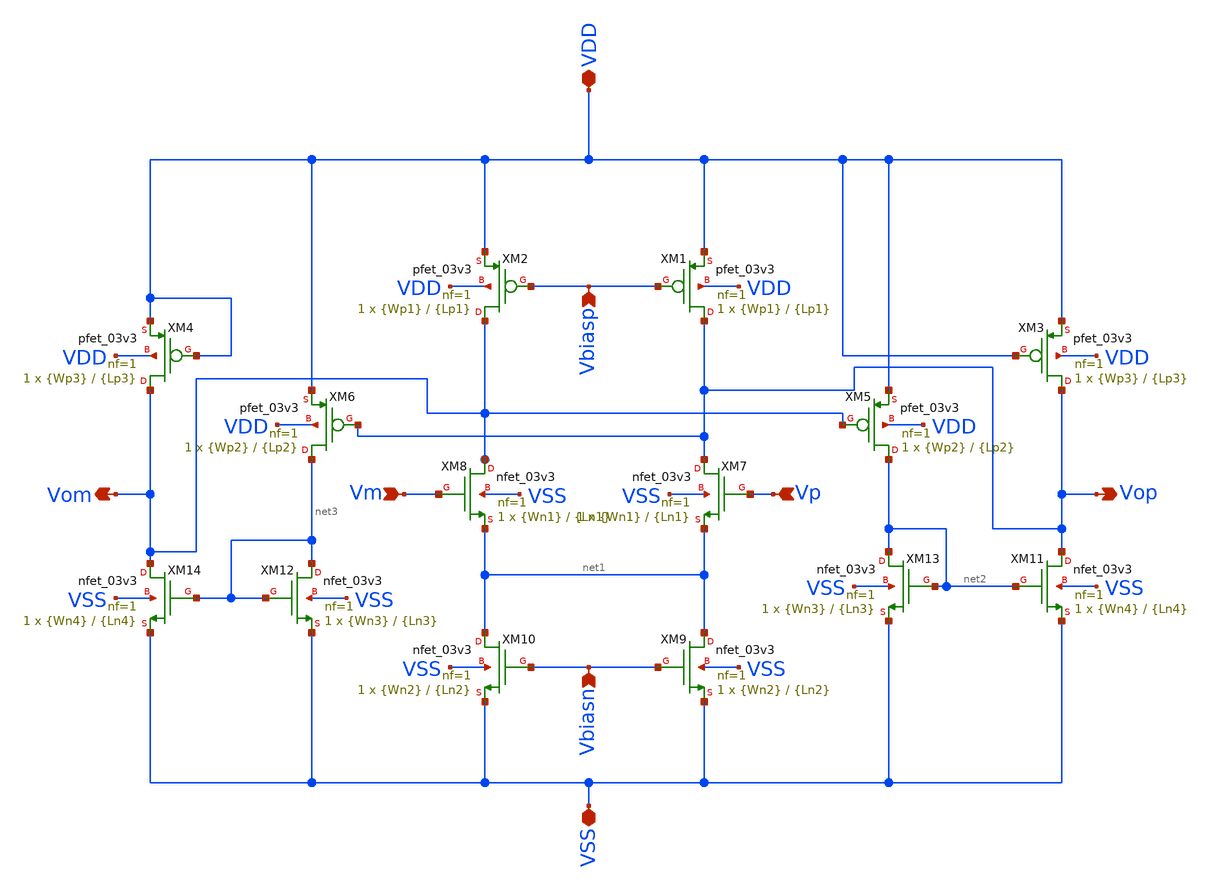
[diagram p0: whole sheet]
** sch_path: src/schematics/fully_differential_amplifier/fullydiffamp.sch
**.subckt fullydiffamp VDD VSS Vbiasn Vbiasp Vm Vp Vom Vop
*.iopin VDD
*.iopin VSS
*.ipin Vbiasn
*.ipin Vbiasp
*.ipin Vm
*.ipin Vp
*.opin Vom
*.opin Vop
XM5 net2 Vom VDD VDD pfet_03v3 L={Lp2} W={Wp2} nf=1 ad='int((nf+1)/2) * W/nf * 0.18u' as='int((nf+2)/2) * W/nf * 0.18u'
+ pd='2*int((nf+1)/2) * (W/nf + 0.18u)' ps='2*int((nf+2)/2) * (W/nf + 0.18u)' nrd='0.18u / W' nrs='0.18u / W'
+ sa=0 sb=0 sd=0 m=1
XM2 Vom Vbiasp VDD VDD pfet_03v3 L={Lp1} W={Wp1} nf=1 ad='int((nf+1)/2) * W/nf * 0.18u' as='int((nf+2)/2) * W/nf * 0.18u'
+ pd='2*int((nf+1)/2) * (W/nf + 0.18u)' ps='2*int((nf+2)/2) * (W/nf + 0.18u)' nrd='0.18u / W' nrs='0.18u / W'
+ sa=0 sb=0 sd=0 m=1
XM8 Vom Vm net1 VSS nfet_03v3 L={Ln1} W={Wn1} nf=1 ad='int((nf+1)/2) * W/nf * 0.18u' as='int((nf+2)/2) * W/nf * 0.18u'
+ pd='2*int((nf+1)/2) * (W/nf + 0.18u)' ps='2*int((nf+2)/2) * (W/nf + 0.18u)' nrd='0.18u / W' nrs='0.18u / W'
+ sa=0 sb=0 sd=0 m=1
XM7 Vop Vp net1 VSS nfet_03v3 L={Ln1} W={Wn1} nf=1 ad='int((nf+1)/2) * W/nf * 0.18u' as='int((nf+2)/2) * W/nf * 0.18u'
+ pd='2*int((nf+1)/2) * (W/nf + 0.18u)' ps='2*int((nf+2)/2) * (W/nf + 0.18u)' nrd='0.18u / W' nrs='0.18u / W'
+ sa=0 sb=0 sd=0 m=1
XM1 Vop Vbiasp VDD VDD pfet_03v3 L={Lp1} W={Wp1} nf=1 ad='int((nf+1)/2) * W/nf * 0.18u' as='int((nf+2)/2) * W/nf * 0.18u'
+ pd='2*int((nf+1)/2) * (W/nf + 0.18u)' ps='2*int((nf+2)/2) * (W/nf + 0.18u)' nrd='0.18u / W' nrs='0.18u / W'
+ sa=0 sb=0 sd=0 m=1
XM6 net3 Vop VDD VDD pfet_03v3 L={Lp2} W={Wp2} nf=1 ad='int((nf+1)/2) * W/nf * 0.18u' as='int((nf+2)/2) * W/nf * 0.18u'
+ pd='2*int((nf+1)/2) * (W/nf + 0.18u)' ps='2*int((nf+2)/2) * (W/nf + 0.18u)' nrd='0.18u / W' nrs='0.18u / W'
+ sa=0 sb=0 sd=0 m=1
XM4 Vom VDD VDD VDD pfet_03v3 L={Lp3} W={Wp3} nf=1 ad='int((nf+1)/2) * W/nf * 0.18u' as='int((nf+2)/2) * W/nf * 0.18u'
+ pd='2*int((nf+1)/2) * (W/nf + 0.18u)' ps='2*int((nf+2)/2) * (W/nf + 0.18u)' nrd='0.18u / W' nrs='0.18u / W'
+ sa=0 sb=0 sd=0 m=1
XM3 Vop VDD VDD VDD pfet_03v3 L={Lp3} W={Wp3} nf=1 ad='int((nf+1)/2) * W/nf * 0.18u' as='int((nf+2)/2) * W/nf * 0.18u'
+ pd='2*int((nf+1)/2) * (W/nf + 0.18u)' ps='2*int((nf+2)/2) * (W/nf + 0.18u)' nrd='0.18u / W' nrs='0.18u / W'
+ sa=0 sb=0 sd=0 m=1
XM9 net1 Vbiasn VSS VSS nfet_03v3 L={Ln2} W={Wn2} nf=1 ad='int((nf+1)/2) * W/nf * 0.18u' as='int((nf+2)/2) * W/nf * 0.18u'
+ pd='2*int((nf+1)/2) * (W/nf + 0.18u)' ps='2*int((nf+2)/2) * (W/nf + 0.18u)' nrd='0.18u / W' nrs='0.18u / W'
+ sa=0 sb=0 sd=0 m=1
XM10 net1 Vbiasn VSS VSS nfet_03v3 L={Ln2} W={Wn2} nf=1 ad='int((nf+1)/2) * W/nf * 0.18u' as='int((nf+2)/2) * W/nf * 0.18u'
+ pd='2*int((nf+1)/2) * (W/nf + 0.18u)' ps='2*int((nf+2)/2) * (W/nf + 0.18u)' nrd='0.18u / W' nrs='0.18u / W'
+ sa=0 sb=0 sd=0 m=1
XM11 Vop net2 VSS VSS nfet_03v3 L={Ln4} W={Wn4} nf=1 ad='int((nf+1)/2) * W/nf * 0.18u' as='int((nf+2)/2) * W/nf * 0.18u'
+ pd='2*int((nf+1)/2) * (W/nf + 0.18u)' ps='2*int((nf+2)/2) * (W/nf + 0.18u)' nrd='0.18u / W' nrs='0.18u / W'
+ sa=0 sb=0 sd=0 m=1
XM13 net2 net2 VSS VSS nfet_03v3 L={Ln3} W={Wn3} nf=1 ad='int((nf+1)/2) * W/nf * 0.18u' as='int((nf+2)/2) * W/nf * 0.18u'
+ pd='2*int((nf+1)/2) * (W/nf + 0.18u)' ps='2*int((nf+2)/2) * (W/nf + 0.18u)' nrd='0.18u / W' nrs='0.18u / W'
+ sa=0 sb=0 sd=0 m=1
XM12 net3 net3 VSS VSS nfet_03v3 L={Ln3} W={Wn3} nf=1 ad='int((nf+1)/2) * W/nf * 0.18u' as='int((nf+2)/2) * W/nf * 0.18u'
+ pd='2*int((nf+1)/2) * (W/nf + 0.18u)' ps='2*int((nf+2)/2) * (W/nf + 0.18u)' nrd='0.18u / W' nrs='0.18u / W'
+ sa=0 sb=0 sd=0 m=1
XM14 Vom net3 VSS VSS nfet_03v3 L={Ln4} W={Wn4} nf=1 ad='int((nf+1)/2) * W/nf * 0.18u' as='int((nf+2)/2) * W/nf * 0.18u'
+ pd='2*int((nf+1)/2) * (W/nf + 0.18u)' ps='2*int((nf+2)/2) * (W/nf + 0.18u)' nrd='0.18u / W' nrs='0.18u / W'
+ sa=0 sb=0 sd=0 m=1
**.ends
.end
